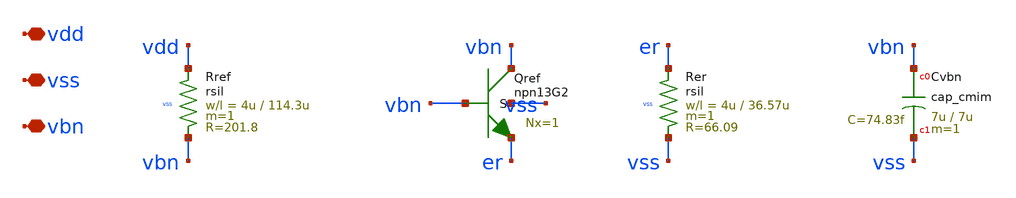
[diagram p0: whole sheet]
** sch_path: design/tx/bias.sch
**.subckt bias vdd vss vbn
*.iopin vdd
*.iopin vss
*.iopin vbn
XRref vdd vbn vss rsil w=4u l=114.3u m=1 mm_ok=1
XQref vbn vbn er vss npn13G2 Nx=1 mm_ok=1
XRer er vss vss rsil w=4u l=36.57u m=1 mm_ok=1
XCvbn vbn vss cap_cmim w=7u l=7u m=1 mm_ok=1
**.ends
.end
